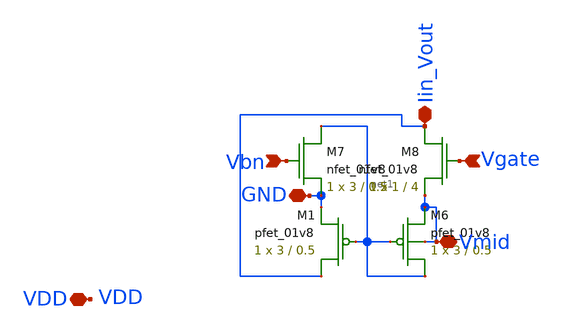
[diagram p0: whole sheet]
** sch_path: final/LDS/IV_converter_LDS.sch
**.subckt IV_converter_LDS Iin_Vout GND Vmid Vbn Vgate VDD
*.iopin Iin_Vout
*.iopin GND
*.iopin Vmid
*.ipin Vbn
*.ipin Vgate
*.iopin VDD
XM6 net1 net1 Vmid Vmid sky130_fd_pr__pfet_01v8 L=0.5 W=3 nf=1 ad='int((nf+1)/2) * W/nf * 0.29' as='int((nf+2)/2) * W/nf * 0.29'
+ pd='2*int((nf+1)/2) * (W/nf + 0.29)' ps='2*int((nf+2)/2) * (W/nf + 0.29)' nrd='0.29 / W' nrs='0.29 / W'
+ sa=0 sb=0 sd=0 mult=1 m=1
XM7 net1 Vbn GND GND sky130_fd_pr__nfet_01v8 L=0.5 W=3 nf=1 ad='int((nf+1)/2) * W/nf * 0.29' as='int((nf+2)/2) * W/nf * 0.29'
+ pd='2*int((nf+1)/2) * (W/nf + 0.29)' ps='2*int((nf+2)/2) * (W/nf + 0.29)' nrd='0.29 / W' nrs='0.29 / W'
+ sa=0 sb=0 sd=0 mult=1 m=1
XM8 Iin_Vout Vgate Vmid GND sky130_fd_pr__nfet_01v8 L=4 W=1 nf=1 ad='int((nf+1)/2) * W/nf * 0.29' as='int((nf+2)/2) * W/nf * 0.29'
+ pd='2*int((nf+1)/2) * (W/nf + 0.29)' ps='2*int((nf+2)/2) * (W/nf + 0.29)' nrd='0.29 / W' nrs='0.29 / W'
+ sa=0 sb=0 sd=0 mult=1 m=1
XM1 Iin_Vout net1 GND VDD sky130_fd_pr__pfet_01v8 L=0.5 W=3 nf=1 ad='int((nf+1)/2) * W/nf * 0.29' as='int((nf+2)/2) * W/nf * 0.29'
+ pd='2*int((nf+1)/2) * (W/nf + 0.29)' ps='2*int((nf+2)/2) * (W/nf + 0.29)' nrd='0.29 / W' nrs='0.29 / W'
+ sa=0 sb=0 sd=0 mult=1 m=1
**.ends
.end
